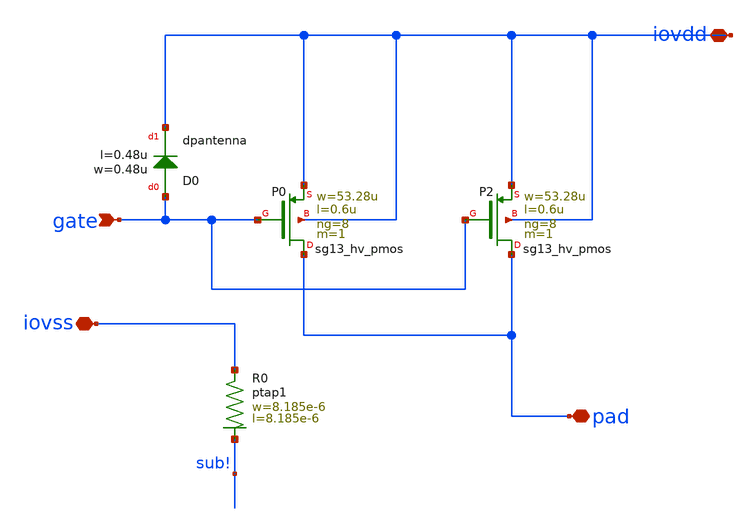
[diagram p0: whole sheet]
** sch_path: ihp-sg13g2/libs.ref/sg13g2_io/sch/xschem/sg13g2_Clamp_P8N8D.sch
**.subckt sg13g2_Clamp_P8N8D iovdd iovss pad gate
*.iopin iovdd
*.iopin iovss
*.iopin pad
*.ipin gate
XP0 pad gate iovdd iovdd sg13_hv_pmos w=53.28u l=0.6u ng=8 m=1 mm_ok=1
XP2 pad gate iovdd iovdd sg13_hv_pmos w=53.28u l=0.6u ng=8 m=1 mm_ok=1
XD0 gate iovdd dpantenna l=0.48u w=0.48u
XR0 iovss sub! ptap1 R=9.826 w=8.185e-6 l=8.185e-6
**.ends
.end
